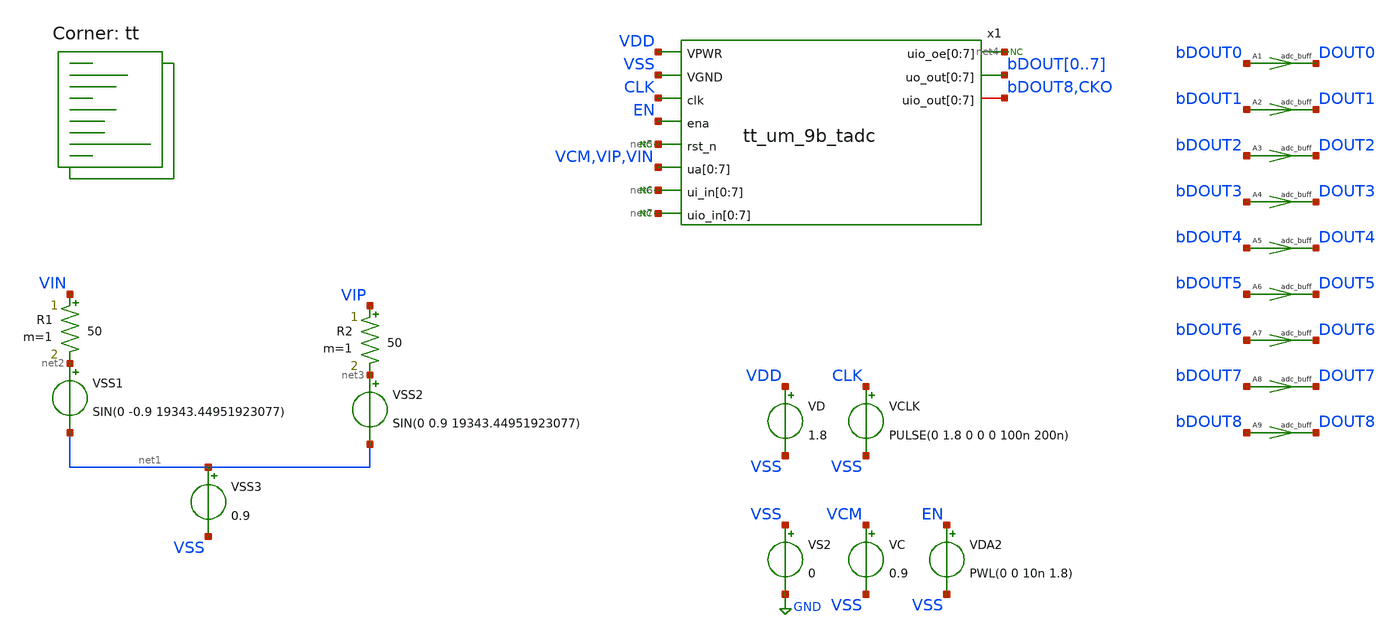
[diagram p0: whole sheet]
** sch_path: xschem/adc_tb.sch
**.subckt adc_tb
VSS1 net2 net1 SIN(0 -0.9 19343.44951923077)
VSS2 net3 net1 SIN(0 0.9 19343.44951923077)
VSS3 net1 VSS 0.9
VCLK CLK VSS PULSE(0 1.8 0 0 0 100n 200n)
R1 VIN net2 50 m=1
R2 VIP net3 50 m=1
VC VCM VSS 0.9
VDA2 EN VSS PWL(0 0 10n 1.8)
A1 [ bDOUT0 ] [ DOUT0 ] adc_buff
A2 [ bDOUT1 ] [ DOUT1 ] adc_buff
A3 [ bDOUT2 ] [ DOUT2 ] adc_buff
A4 [ bDOUT3 ] [ DOUT3 ] adc_buff
A5 [ bDOUT4 ] [ DOUT4 ] adc_buff
A6 [ bDOUT5 ] [ DOUT5 ] adc_buff
A7 [ bDOUT6 ] [ DOUT6 ] adc_buff
A8 [ bDOUT7 ] [ DOUT7 ] adc_buff
VS2 VSS GND 0
VD VDD VSS 1.8
A9 [ bDOUT8 ] [ DOUT8 ] adc_buff
x1 VDD VSS net4[7] net4[6] net4[5] net4[4] net4[3] net4[2] net4[1] net4[0] CLK EN bDOUT0 bDOUT1
+ bDOUT2 bDOUT3 bDOUT4 bDOUT5 bDOUT6 bDOUT7 net5 bDOUT8 CKO bDOUT8 CKO bDOUT8 CKO bDOUT8 CKO VCM VIP VIN VCM
+ VIP VIN VCM VIP net6[7] net6[6] net6[5] net6[4] net6[3] net6[2] net6[1] net6[0] net7[7] net7[6] net7[5]
+ net7[4] net7[3] net7[2] net7[1] net7[0] tt_um_9b_tadc
* noconn #net5
* noconn #net4
* noconn #net6
* noconn #net7
**** begin user architecture code

** opencircuitdesign pdks install
* .lib $::SKYWATER_MODELS/sky130.lib.spice tt
*.include $PDK_ROOT/$PDK/libs.ref/sky130_fd_sc_hdll/spice/sky130_fd_sc_hdll.spice
.include $PDK_ROOT/$PDK/libs.ref/sky130_fd_sc_hs/spice/sky130_fd_sc_hs.spice
.include $PDK_ROOT/$PDK/libs.ref/sky130_fd_sc_hd/spice/sky130_fd_sc_hd.spice



.option wnflag=0 bypass=1
.options method=trap rawfile=binary
.options solver=klu nomod
Eout out 0 VALUE = { ((V(dout0)*256 + V(dout1)*128 + V(dout2)*64 + V(dout3)*32 + V(dout4)*16 + V(dout5)*8 + V(dout6)*4 + V(dout7)*2 + V(dout8)*1)/3.3) - 256 }
Epowa pow 0 VALUE = { V(vdd)*(-i(vd)) }
.model adc_buff adc_bridge(in_low=0.18 in_high=1.62 rise_delay=100p fall_delay=100p)
.control
global netlist_dir .
set num_threads=16
save cko out pow vip vin x1.vcp x1.vcn 'x1.cf[0]' 'x1.cf[1]' 'x1.cf[2]' 'x1.cf[3]' 'x1.cf[4]' 'x1.cf[5]'
+ 'x1.cf[6]' 'x1.cf[7]' 'x1.cf[8]'
tran 10n 5350u 0 ; Mengubah start time menjadi 10n
rusage traniter trantime
meas tran avg_pow  AVG pow from=1n to=535u
remzerovec
write adc8b_tb_dynamic.raw
wrdata adc8b_tb_dynamic.txt out cko pow_a pow_d pow_r vip vin
quit 1
.endc


.lib $::SKYWATER_MODELS/sky130.lib.spice tt
**** end user architecture code
**.ends
.GLOBAL GND
.end
